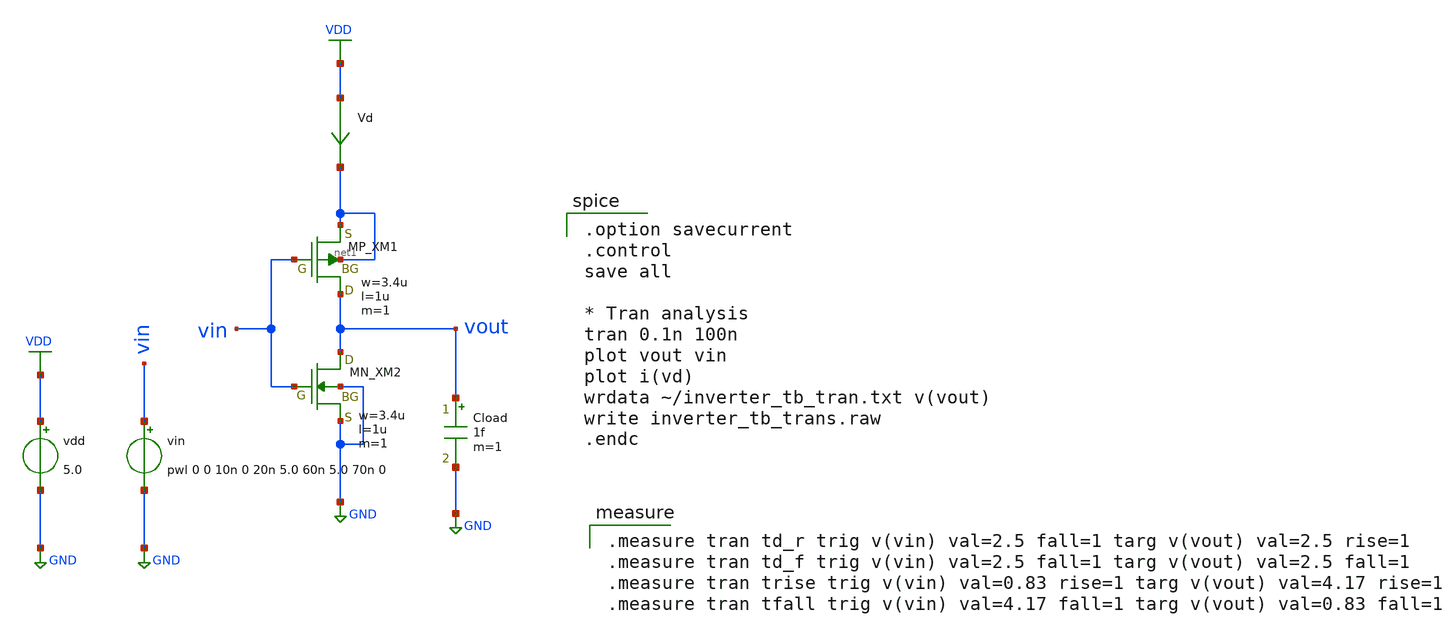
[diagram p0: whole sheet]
** sch_path: inverter_sim_tran.sch
**.subckt inverter_sim_tran
XM1 vout vin net1 net1 PMOS w=3.4u l=1u as=0 ad=0 ps=0 pd=0 nrd=0 nrs=0 m=1
XM2 vout vin GND GND NMOS w=3.4u l=1u as=0 ad=0 ps=0 pd=0 nrd=0 nrs=0 m=1
vdd VDD GND 5.0
vin vin GND pwl 0 0 10n 0 20n 5.0 60n 5.0 70n 0
Cload vout GND 1f m=1
Vd VDD net1 0
.save i(vd)
**** begin user architecture code
 .include $::LIB/../ip62_models

.option savecurrent
.control
save all

* Tran analysis
tran 0.1n 100n
plot vout vin
plot i(vd)
wrdata ~/inverter_tb_tran.txt v(vout)
write inverter_tb_trans.raw
.endc


.measure tran td_r trig v(vin) val=2.5 fall=1 targ v(vout) val=2.5 rise=1
.measure tran td_f trig v(vin) val=2.5 fall=1 targ v(vout) val=2.5 fall=1
.measure tran trise trig v(vin) val=0.83 rise=1 targ v(vout) val=4.17 rise=1
.measure tran tfall trig v(vin) val=4.17 fall=1 targ v(vout) val=0.83 fall=1

**** end user architecture code
**.ends
.GLOBAL VDD
.GLOBAL GND
.end
